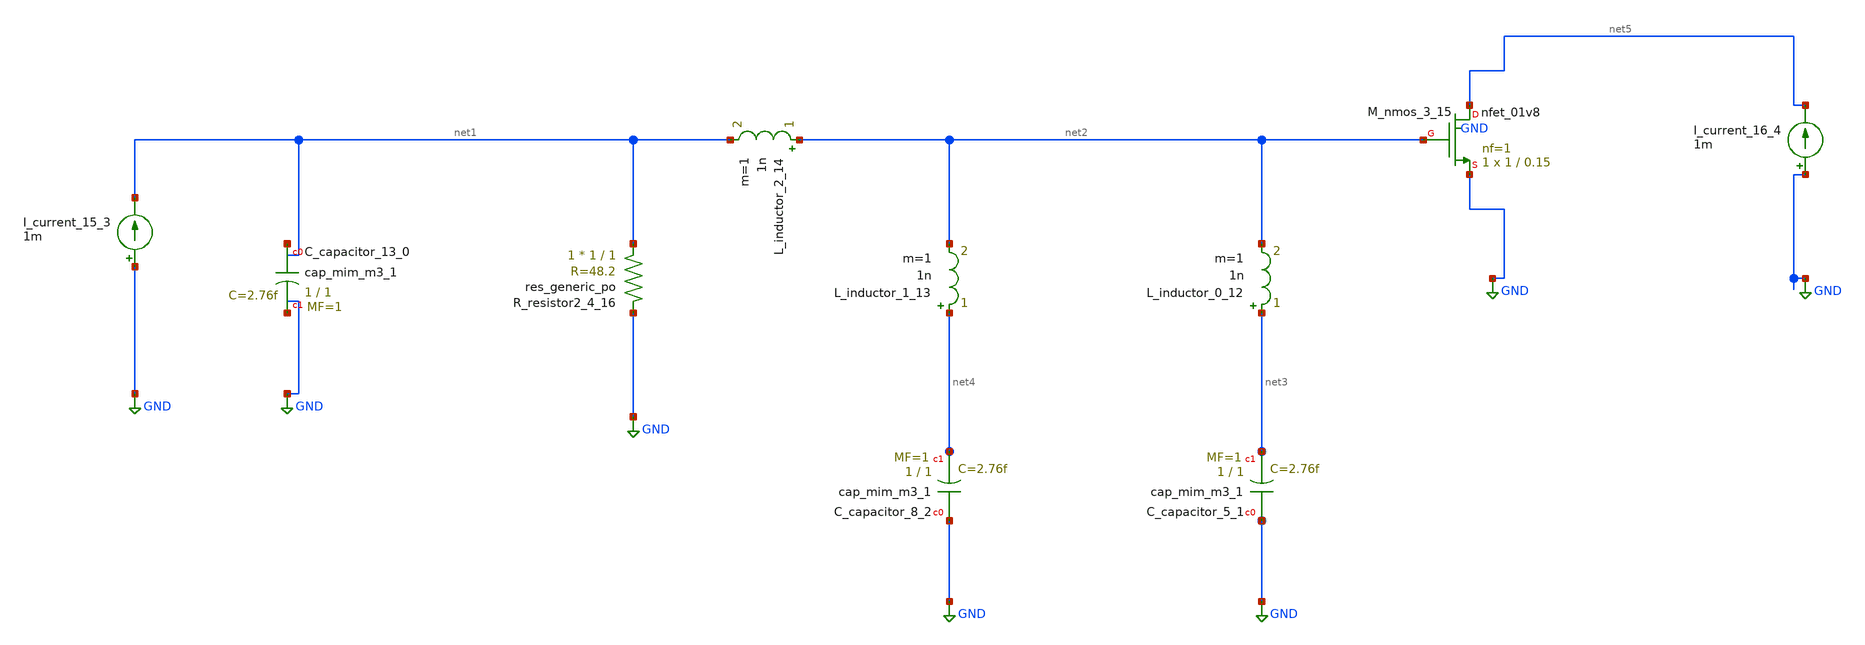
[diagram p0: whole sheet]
** sch_path: schematics/SchemGen/10_1109_OJCAS_2022_3164396_05_003.sch
**.subckt 10_1109_OJCAS_2022_3164396_05_003
XC_capacitor_13_0 net1 GND sky130_fd_pr__cap_mim_m3_1 W=1 L=1 MF=1 m=1
XC_capacitor_5_1 GND net3 sky130_fd_pr__cap_mim_m3_1 W=1 L=1 MF=1 m=1
XC_capacitor_8_2 GND net4 sky130_fd_pr__cap_mim_m3_1 W=1 L=1 MF=1 m=1
I_current_15_3 GND net1 1m
I_current_16_4 GND net5 1m
L_inductor_0_12 net3 net2 1n m=1
L_inductor_1_13 net4 net2 1n m=1
L_inductor_2_14 net2 net1 1n m=1
XM_nmos_3_15 net5 net2 GND GND sky130_fd_pr__nfet_01v8 L=0.15 W=1 nf=1 ad='int((1 + 1)/2) * 1 / 1 * 0.29'
+ as='int((1 + 2)/2) * 1 / 1 * 0.29' pd='2*int((1 + 1)/2) * (1 / 1 + 0.29)' ps='2*int((1 + 2)/2) * (1 / 1 + 0.29)'
+ nrd='0.29 / 1 ' nrs='0.29 / 1 ' sa=0 sb=0 sd=0 mult=1 m=1
XR_resistor2_4_16 net1 GND sky130_fd_pr__res_generic_po W=1 L=1 m=1
**.ends
.GLOBAL GND
.end
